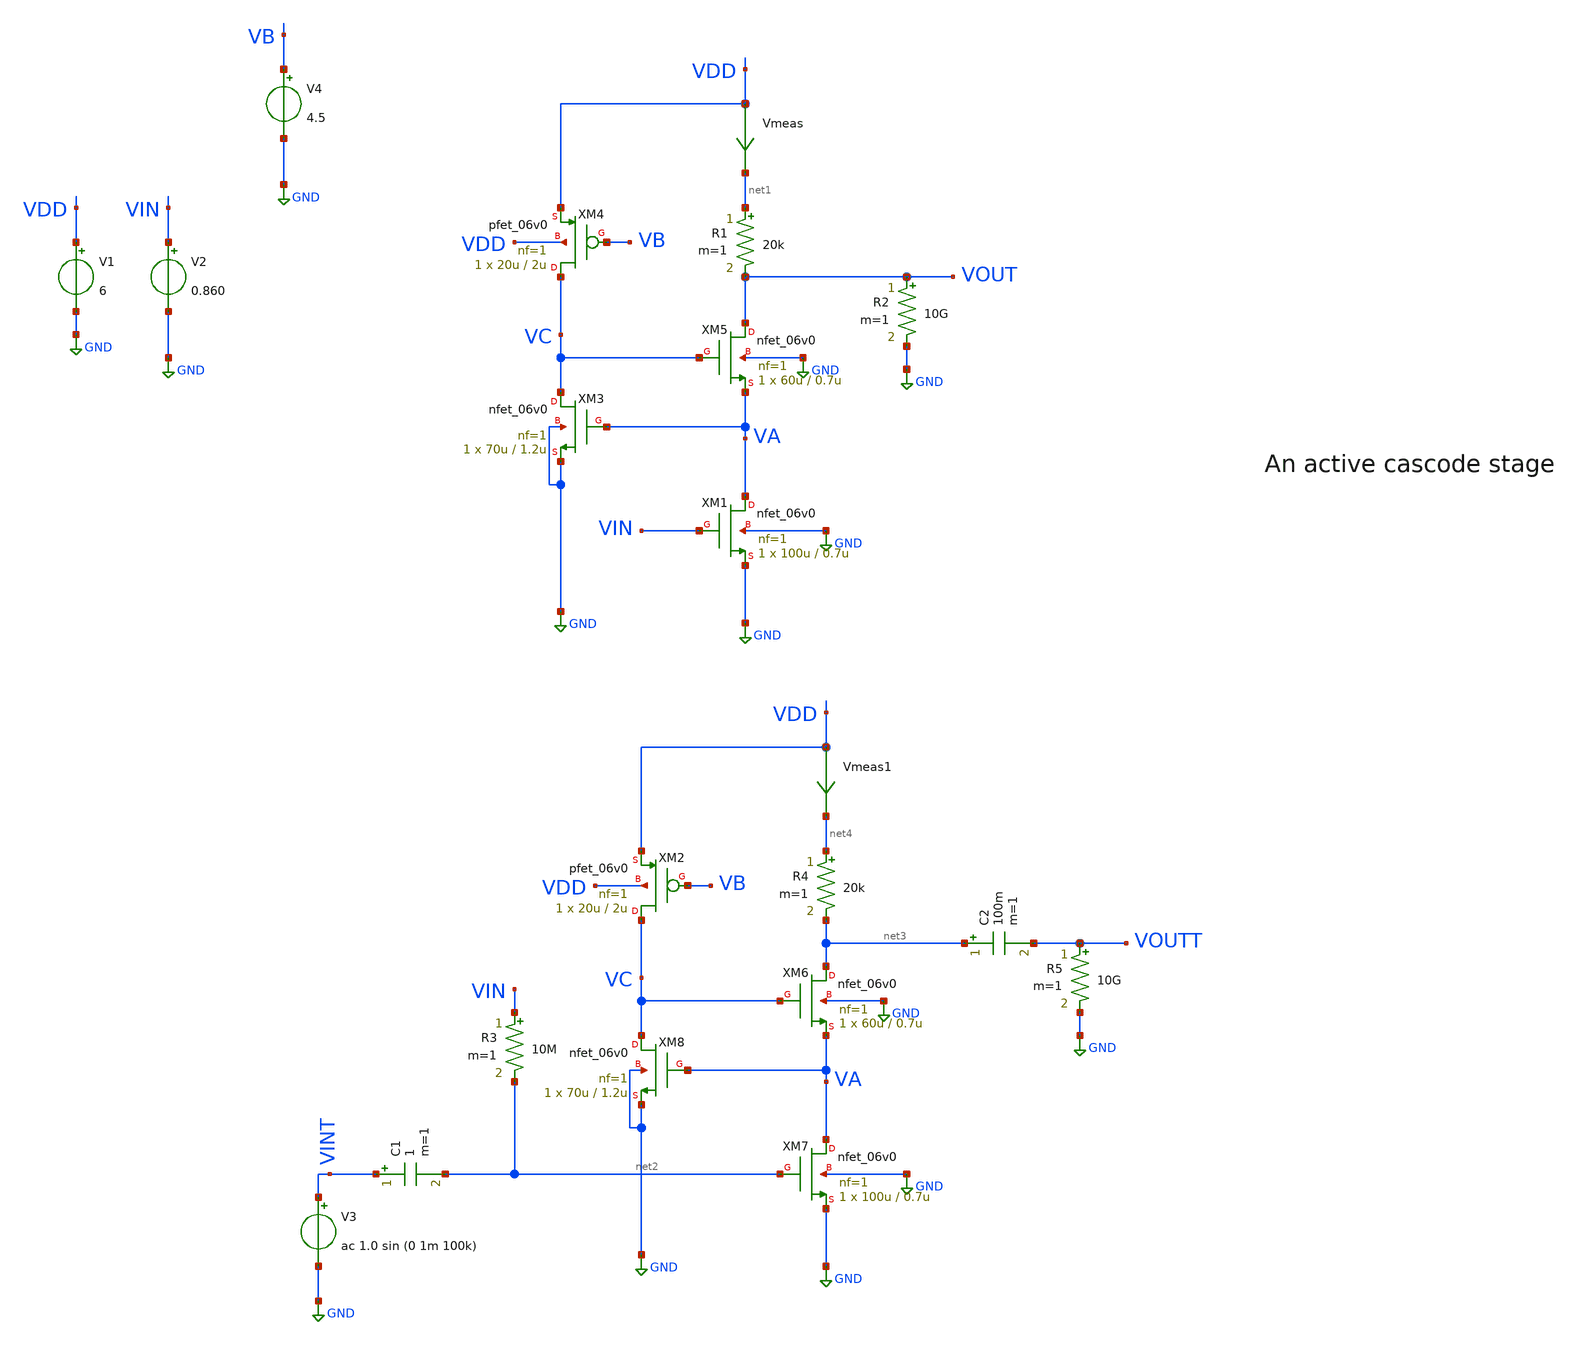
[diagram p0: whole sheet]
** sch_path: basic_circuits/active_cascode.sch
**.subckt active_cascode
Vmeas VDD net1 0
.save i(vmeas)
V1 VDD GND 6
V2 VIN GND 0.860
V3 VINT GND ac 1.0 sin (0 1m 100k)
R1 net1 VOUT 20k m=1
R2 VOUT GND 10G m=1
C1 VINT net2 1 m=1
R3 VIN net2 10M m=1
C2 net3 VOUTT 100m m=1
R5 VOUTT GND 10G m=1
XM4 VC VB VDD VDD pfet_06v0 L=2u W=20u nf=1 ad='int((nf+1)/2) * W/nf * 0.18u' as='int((nf+2)/2) * W/nf * 0.18u'
+ pd='2*int((nf+1)/2) * (W/nf + 0.18u)' ps='2*int((nf+2)/2) * (W/nf + 0.18u)' nrd='0.18u / W' nrs='0.18u / W'
+ sa=0 sb=0 sd=0 m=1
XM5 VOUT VC VA GND nfet_06v0 L=0.7u W=60u nf=1 ad='int((nf+1)/2) * W/nf * 0.18u' as='int((nf+2)/2) * W/nf * 0.18u'
+ pd='2*int((nf+1)/2) * (W/nf + 0.18u)' ps='2*int((nf+2)/2) * (W/nf + 0.18u)' nrd='0.18u / W' nrs='0.18u / W'
+ sa=0 sb=0 sd=0 m=1
XM1 VA VIN GND GND nfet_06v0 L=0.7u W=100u nf=1 ad='int((nf+1)/2) * W/nf * 0.18u' as='int((nf+2)/2) * W/nf * 0.18u'
+ pd='2*int((nf+1)/2) * (W/nf + 0.18u)' ps='2*int((nf+2)/2) * (W/nf + 0.18u)' nrd='0.18u / W' nrs='0.18u / W'
+ sa=0 sb=0 sd=0 m=1
V4 VB GND 4.5
XM3 VC VA GND GND nfet_06v0 L=1.2u W=70u nf=1 ad='int((nf+1)/2) * W/nf * 0.18u' as='int((nf+2)/2) * W/nf * 0.18u'
+ pd='2*int((nf+1)/2) * (W/nf + 0.18u)' ps='2*int((nf+2)/2) * (W/nf + 0.18u)' nrd='0.18u / W' nrs='0.18u / W'
+ sa=0 sb=0 sd=0 m=1
Vmeas1 VDD net4 0
.save i(vmeas1)
R4 net4 net3 20k m=1
XM2 VC VB VDD VDD pfet_06v0 L=2u W=20u nf=1 ad='int((nf+1)/2) * W/nf * 0.18u' as='int((nf+2)/2) * W/nf * 0.18u'
+ pd='2*int((nf+1)/2) * (W/nf + 0.18u)' ps='2*int((nf+2)/2) * (W/nf + 0.18u)' nrd='0.18u / W' nrs='0.18u / W'
+ sa=0 sb=0 sd=0 m=1
XM6 net3 VC VA GND nfet_06v0 L=0.7u W=60u nf=1 ad='int((nf+1)/2) * W/nf * 0.18u' as='int((nf+2)/2) * W/nf * 0.18u'
+ pd='2*int((nf+1)/2) * (W/nf + 0.18u)' ps='2*int((nf+2)/2) * (W/nf + 0.18u)' nrd='0.18u / W' nrs='0.18u / W'
+ sa=0 sb=0 sd=0 m=1
XM7 VA net2 GND GND nfet_06v0 L=0.7u W=100u nf=1 ad='int((nf+1)/2) * W/nf * 0.18u' as='int((nf+2)/2) * W/nf * 0.18u'
+ pd='2*int((nf+1)/2) * (W/nf + 0.18u)' ps='2*int((nf+2)/2) * (W/nf + 0.18u)' nrd='0.18u / W' nrs='0.18u / W'
+ sa=0 sb=0 sd=0 m=1
XM8 VC VA GND GND nfet_06v0 L=1.2u W=70u nf=1 ad='int((nf+1)/2) * W/nf * 0.18u' as='int((nf+2)/2) * W/nf * 0.18u'
+ pd='2*int((nf+1)/2) * (W/nf + 0.18u)' ps='2*int((nf+2)/2) * (W/nf + 0.18u)' nrd='0.18u / W' nrs='0.18u / W'
+ sa=0 sb=0 sd=0 m=1
**** begin user architecture code

**************************************************************
**************************************************************
**************************************************************
**************************************************************
**************************************************************
*LIBs*********************************************************
**************************************************************
**************************************************************
**************************************************************
**************************************************************
**************************************************************
.include $::180MCU_MODELS/design.ngspice
*.lib $::180MCU_MODELS/sm141064.ngspice statistical *use statistical if you want global and parameter mismatch
*.lib $::180MCU_MODELS/sm141064.ngspice res_statistical
.lib $::180MCU_MODELS/sm141064.ngspice typical
.lib $::180MCU_MODELS/sm141064.ngspice res_typical
.lib $::180MCU_MODELS/sm141064.ngspice moscap_typical
.lib $::180MCU_MODELS/sm141064.ngspice bjt_typical
.lib $::180MCU_MODELS/sm141064.ngspice diode_typical
.lib $::180MCU_MODELS/sm141064.ngspice mimcap_typical
**************************************************************
**************************************************************
**************************************************************
**************************************************************
**************************************************************
*Corners/montecarlo options***********************************
**************************************************************
**************************************************************
**************************************************************
**************************************************************
**************************************************************
.TEMP 27
.param   sw_stat_global = 1   sw_stat_mism = 1  mc_skew = 3  res_mc_skew = 3  cap_mc_skew = 3
+  fnoicor = 1
**************************************************************
**************************************************************
**************************************************************
**************************************************************
*SIMULATION and Plots*****************************************
**************************************************************
**************************************************************
**************************************************************
**************************************************************
.control
save all
dc V2 0 6 0.01
*dc simulation
plot v(VOUT) v(VIN) deriv(v(VOUT)) v(VA) v(VC)
*ploting VIN VOUT and the voltage gain
plot i(Vmeas)
*ploting the current for curiosity
tran 1ns 20u
*transient simulation
plot (v(VINT)) (v(VOUTT))
*simple plot to exemplify the gain
fft v(VOUTT) v(VINT)
*fast fourier transfor
plot mag(v(VOUTT)) mag(v(VINT))
* analyse the frequency spectrum of the transient waves, to detect distortion
ac dec 20 1 50G
*simple ac simulation
plot v(VOUTT)
*gain in function of the input frequency
.endc

**** end user architecture code
**.ends
.GLOBAL GND
.end
